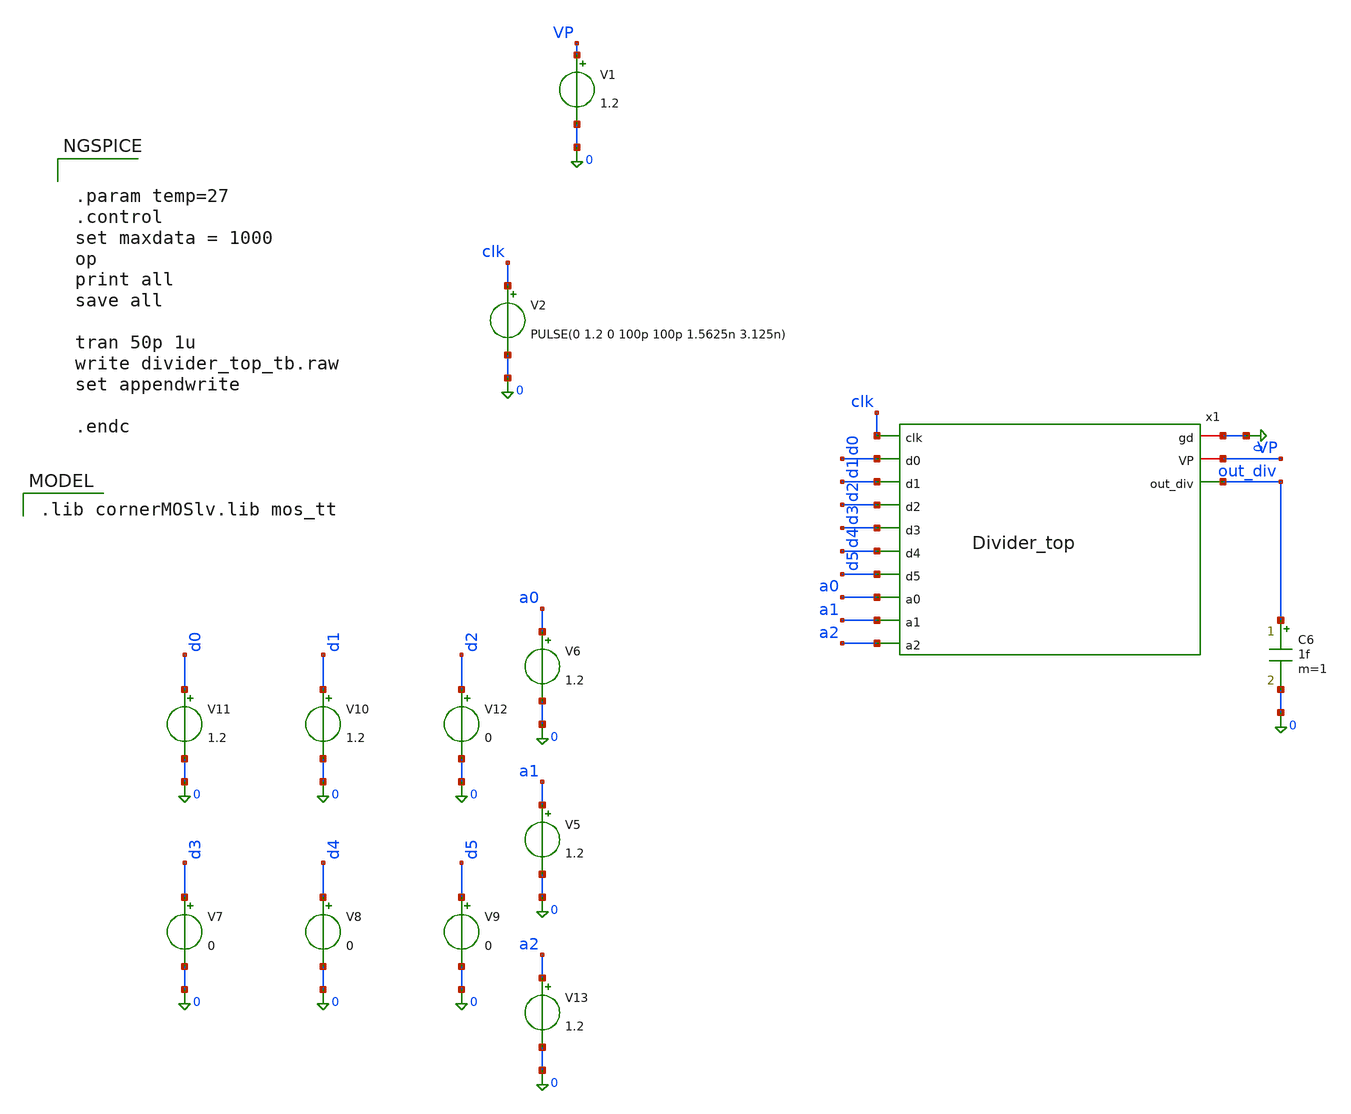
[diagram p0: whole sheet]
** sch_path: schematics/divider/tb/divider_top_tb.sch
**.subckt divider_top_tb
V1 VP 0 1.2
V2 clk 0 PULSE(0 1.2 0 100p 100p 1.5625n 3.125n)
V8 d4 0 0
V9 d5 0 0
V11 d0 0 1.2
V10 d1 0 1.2
V12 d2 0 0
V7 d3 0 0
V5 a1 0 1.2
V6 a0 0 1.2
V13 a2 0 1.2
x1 0 VP clk d0 d1 d2 d3 d4 d5 a0 a1 a2 out_div Divider_top
C6 out_div 0 1f m=1
**** begin user architecture code


.param temp=27
.control
set maxdata = 1000
op
print all
save all

tran 50p 1u
write divider_top_tb.raw
set appendwrite

.endc


 .lib cornerMOSlv.lib mos_tt

**** end user architecture code
**.ends
.end
